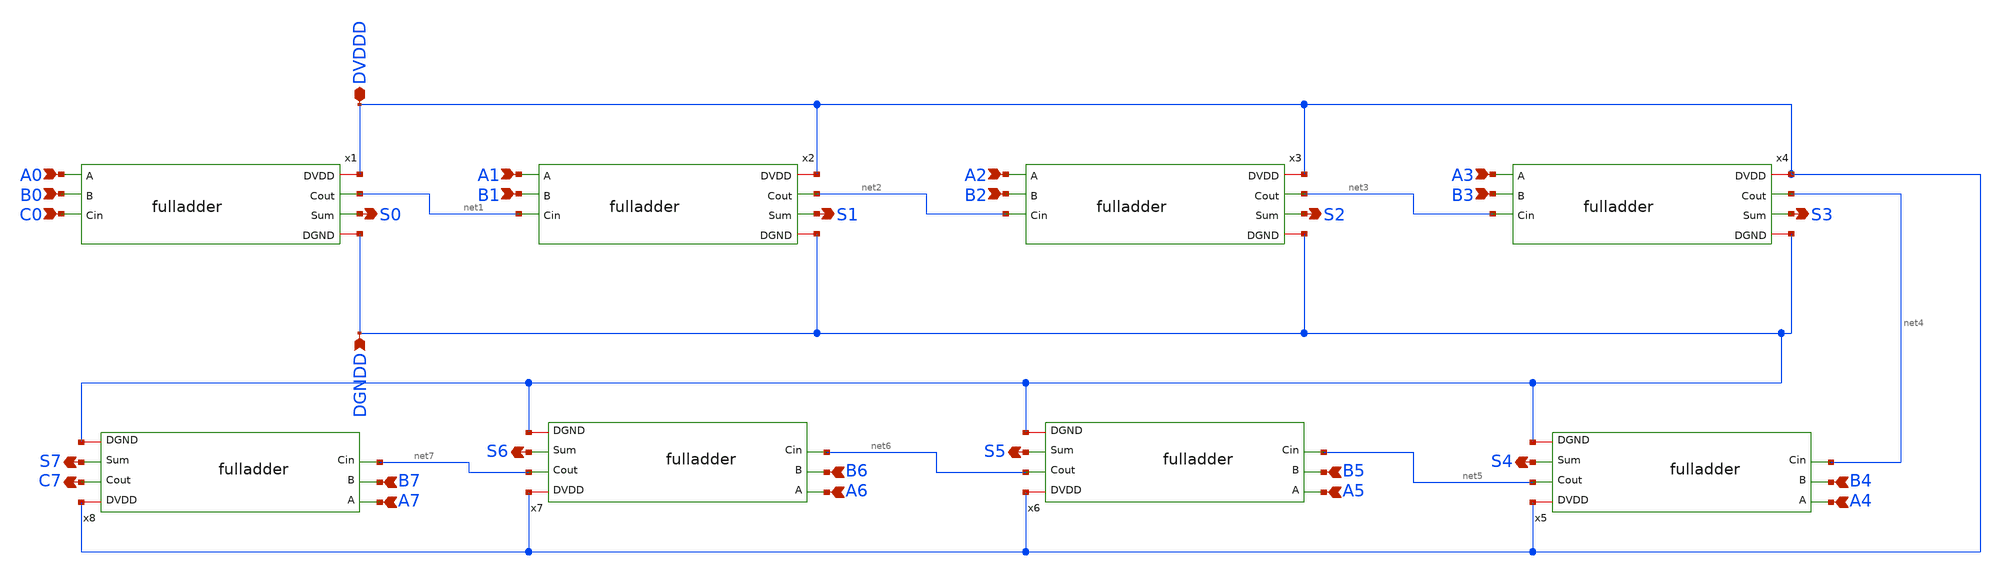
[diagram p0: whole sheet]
** sch_path: Tutorial_6/Part-B/rippleadder.sch
**.subckt rippleadder DVDDD DGNDD S0 S1 S2 S3 S4 S5 S6 S7 A0 A1 A2 A3 A4 A5 A6 A7 B1 B2 B0 B3 B4 B5
*+ B6 B7 C0 C7
*.iopin DVDDD
*.ipin DGNDD
*.opin S0
*.opin S1
*.opin S2
*.opin S3
*.opin S4
*.opin S5
*.opin S6
*.opin S7
*.ipin A0
*.ipin A1
*.ipin A2
*.ipin A3
*.ipin A4
*.ipin A5
*.ipin A6
*.ipin A7
*.ipin B1
*.ipin B2
*.ipin B0
*.ipin B3
*.ipin B4
*.ipin B5
*.ipin B6
*.ipin B7
*.ipin C0
*.opin C7
x1 DVDDD A0 B0 C0 net1 S0 DGNDD fulladder
x2 DVDDD A1 B1 net1 net2 S1 DGNDD fulladder
x3 DVDDD A2 B2 net2 net3 S2 DGNDD fulladder
x4 DVDDD A3 B3 net3 net4 S3 DGNDD fulladder
x5 DVDDD A4 B4 net4 net5 S4 DGNDD fulladder
x6 DVDDD A5 B5 net5 net6 S5 DGNDD fulladder
x7 DVDDD A6 B6 net6 net7 S6 DGNDD fulladder
x8 DVDDD A7 B7 net7 C7 S7 DGNDD fulladder
**.ends

* expanding   symbol:  fulladder.sym # of pins=7
** sym_path: Tutorial_6/Part-B/fulladder.sym
** sch_path: Tutorial_6/Part-B/fulladder.sch
.subckt fulladder DVDD A B Cin Cout Sum DGND
*.opin Cout
*.opin Sum
*.ipin A
*.ipin B
*.ipin Cin
*.iopin DVDD
*.iopin DGND
XM25 net3 A DVDD DVDD sky130_fd_pr__pfet_01v8 L=0.15 W=0.84 nf=1 ad='int((nf+1)/2) * W/nf * 0.29' as='int((nf+2)/2) * W/nf * 0.29'
+ pd='2*int((nf+1)/2) * (W/nf + 0.29)' ps='2*int((nf+2)/2) * (W/nf + 0.29)' nrd='0.29 / W' nrs='0.29 / W'
+ sa=0 sb=0 sd=0 mult=1 m=1
XM26 net3 A DVDD DVDD sky130_fd_pr__pfet_01v8 L=0.15 W=0.84 nf=1 ad='int((nf+1)/2) * W/nf * 0.29' as='int((nf+2)/2) * W/nf * 0.29'
+ pd='2*int((nf+1)/2) * (W/nf + 0.29)' ps='2*int((nf+2)/2) * (W/nf + 0.29)' nrd='0.29 / W' nrs='0.29 / W'
+ sa=0 sb=0 sd=0 mult=1 m=1
XM27 net2 A DVDD DVDD sky130_fd_pr__pfet_01v8 L=0.15 W=0.84 nf=1 ad='int((nf+1)/2) * W/nf * 0.29' as='int((nf+2)/2) * W/nf * 0.29'
+ pd='2*int((nf+1)/2) * (W/nf + 0.29)' ps='2*int((nf+2)/2) * (W/nf + 0.29)' nrd='0.29 / W' nrs='0.29 / W'
+ sa=0 sb=0 sd=0 mult=1 m=1
XM28 net2 A DVDD DVDD sky130_fd_pr__pfet_01v8 L=0.15 W=0.84 nf=1 ad='int((nf+1)/2) * W/nf * 0.29' as='int((nf+2)/2) * W/nf * 0.29'
+ pd='2*int((nf+1)/2) * (W/nf + 0.29)' ps='2*int((nf+2)/2) * (W/nf + 0.29)' nrd='0.29 / W' nrs='0.29 / W'
+ sa=0 sb=0 sd=0 mult=1 m=1
XM29 net2 B DVDD DVDD sky130_fd_pr__pfet_01v8 L=0.15 W=0.84 nf=1 ad='int((nf+1)/2) * W/nf * 0.29' as='int((nf+2)/2) * W/nf * 0.29'
+ pd='2*int((nf+1)/2) * (W/nf + 0.29)' ps='2*int((nf+2)/2) * (W/nf + 0.29)' nrd='0.29 / W' nrs='0.29 / W'
+ sa=0 sb=0 sd=0 mult=1 m=1
XM30 net2 B DVDD DVDD sky130_fd_pr__pfet_01v8 L=0.15 W=0.84 nf=1 ad='int((nf+1)/2) * W/nf * 0.29' as='int((nf+2)/2) * W/nf * 0.29'
+ pd='2*int((nf+1)/2) * (W/nf + 0.29)' ps='2*int((nf+2)/2) * (W/nf + 0.29)' nrd='0.29 / W' nrs='0.29 / W'
+ sa=0 sb=0 sd=0 mult=1 m=1
XM31 Cout B net3 DVDD sky130_fd_pr__pfet_01v8 L=0.15 W=0.84 nf=1 ad='int((nf+1)/2) * W/nf * 0.29' as='int((nf+2)/2) * W/nf * 0.29'
+ pd='2*int((nf+1)/2) * (W/nf + 0.29)' ps='2*int((nf+2)/2) * (W/nf + 0.29)' nrd='0.29 / W' nrs='0.29 / W'
+ sa=0 sb=0 sd=0 mult=1 m=1
XM32 Cout B net3 DVDD sky130_fd_pr__pfet_01v8 L=0.15 W=0.84 nf=1 ad='int((nf+1)/2) * W/nf * 0.29' as='int((nf+2)/2) * W/nf * 0.29'
+ pd='2*int((nf+1)/2) * (W/nf + 0.29)' ps='2*int((nf+2)/2) * (W/nf + 0.29)' nrd='0.29 / W' nrs='0.29 / W'
+ sa=0 sb=0 sd=0 mult=1 m=1
XM33 Cout Cin net2 DVDD sky130_fd_pr__pfet_01v8 L=0.15 W=0.84 nf=1 ad='int((nf+1)/2) * W/nf * 0.29' as='int((nf+2)/2) * W/nf * 0.29'
+ pd='2*int((nf+1)/2) * (W/nf + 0.29)' ps='2*int((nf+2)/2) * (W/nf + 0.29)' nrd='0.29 / W' nrs='0.29 / W'
+ sa=0 sb=0 sd=0 mult=1 m=1
XM34 Cout Cin net2 DVDD sky130_fd_pr__pfet_01v8 L=0.15 W=0.84 nf=1 ad='int((nf+1)/2) * W/nf * 0.29' as='int((nf+2)/2) * W/nf * 0.29'
+ pd='2*int((nf+1)/2) * (W/nf + 0.29)' ps='2*int((nf+2)/2) * (W/nf + 0.29)' nrd='0.29 / W' nrs='0.29 / W'
+ sa=0 sb=0 sd=0 mult=1 m=1
XM35 net6 A DVDD DVDD sky130_fd_pr__pfet_01v8 L=0.15 W=0.84 nf=1 ad='int((nf+1)/2) * W/nf * 0.29' as='int((nf+2)/2) * W/nf * 0.29'
+ pd='2*int((nf+1)/2) * (W/nf + 0.29)' ps='2*int((nf+2)/2) * (W/nf + 0.29)' nrd='0.29 / W' nrs='0.29 / W'
+ sa=0 sb=0 sd=0 mult=1 m=1
XM36 net6 A DVDD DVDD sky130_fd_pr__pfet_01v8 L=0.15 W=0.84 nf=1 ad='int((nf+1)/2) * W/nf * 0.29' as='int((nf+2)/2) * W/nf * 0.29'
+ pd='2*int((nf+1)/2) * (W/nf + 0.29)' ps='2*int((nf+2)/2) * (W/nf + 0.29)' nrd='0.29 / W' nrs='0.29 / W'
+ sa=0 sb=0 sd=0 mult=1 m=1
XM37 net6 B DVDD DVDD sky130_fd_pr__pfet_01v8 L=0.15 W=0.84 nf=1 ad='int((nf+1)/2) * W/nf * 0.29' as='int((nf+2)/2) * W/nf * 0.29'
+ pd='2*int((nf+1)/2) * (W/nf + 0.29)' ps='2*int((nf+2)/2) * (W/nf + 0.29)' nrd='0.29 / W' nrs='0.29 / W'
+ sa=0 sb=0 sd=0 mult=1 m=1
XM38 net6 B DVDD DVDD sky130_fd_pr__pfet_01v8 L=0.15 W=0.84 nf=1 ad='int((nf+1)/2) * W/nf * 0.29' as='int((nf+2)/2) * W/nf * 0.29'
+ pd='2*int((nf+1)/2) * (W/nf + 0.29)' ps='2*int((nf+2)/2) * (W/nf + 0.29)' nrd='0.29 / W' nrs='0.29 / W'
+ sa=0 sb=0 sd=0 mult=1 m=1
XM39 net6 Cin DVDD DVDD sky130_fd_pr__pfet_01v8 L=0.15 W=0.84 nf=1 ad='int((nf+1)/2) * W/nf * 0.29' as='int((nf+2)/2) * W/nf * 0.29'
+ pd='2*int((nf+1)/2) * (W/nf + 0.29)' ps='2*int((nf+2)/2) * (W/nf + 0.29)' nrd='0.29 / W' nrs='0.29 / W'
+ sa=0 sb=0 sd=0 mult=1 m=1
XM40 net6 Cin DVDD DVDD sky130_fd_pr__pfet_01v8 L=0.15 W=0.84 nf=1 ad='int((nf+1)/2) * W/nf * 0.29' as='int((nf+2)/2) * W/nf * 0.29'
+ pd='2*int((nf+1)/2) * (W/nf + 0.29)' ps='2*int((nf+2)/2) * (W/nf + 0.29)' nrd='0.29 / W' nrs='0.29 / W'
+ sa=0 sb=0 sd=0 mult=1 m=1
XM41 Sum Cout net6 DVDD sky130_fd_pr__pfet_01v8 L=0.15 W=0.84 nf=1 ad='int((nf+1)/2) * W/nf * 0.29' as='int((nf+2)/2) * W/nf * 0.29'
+ pd='2*int((nf+1)/2) * (W/nf + 0.29)' ps='2*int((nf+2)/2) * (W/nf + 0.29)' nrd='0.29 / W' nrs='0.29 / W'
+ sa=0 sb=0 sd=0 mult=1 m=1
XM42 Sum Cout net6 DVDD sky130_fd_pr__pfet_01v8 L=0.15 W=0.84 nf=1 ad='int((nf+1)/2) * W/nf * 0.29' as='int((nf+2)/2) * W/nf * 0.29'
+ pd='2*int((nf+1)/2) * (W/nf + 0.29)' ps='2*int((nf+2)/2) * (W/nf + 0.29)' nrd='0.29 / W' nrs='0.29 / W'
+ sa=0 sb=0 sd=0 mult=1 m=1
XM43 net7 A DVDD DVDD sky130_fd_pr__pfet_01v8 L=0.15 W=0.84 nf=1 ad='int((nf+1)/2) * W/nf * 0.29' as='int((nf+2)/2) * W/nf * 0.29'
+ pd='2*int((nf+1)/2) * (W/nf + 0.29)' ps='2*int((nf+2)/2) * (W/nf + 0.29)' nrd='0.29 / W' nrs='0.29 / W'
+ sa=0 sb=0 sd=0 mult=1 m=1
XM44 net7 A DVDD DVDD sky130_fd_pr__pfet_01v8 L=0.15 W=0.84 nf=1 ad='int((nf+1)/2) * W/nf * 0.29' as='int((nf+2)/2) * W/nf * 0.29'
+ pd='2*int((nf+1)/2) * (W/nf + 0.29)' ps='2*int((nf+2)/2) * (W/nf + 0.29)' nrd='0.29 / W' nrs='0.29 / W'
+ sa=0 sb=0 sd=0 mult=1 m=1
XM45 net7 A DVDD DVDD sky130_fd_pr__pfet_01v8 L=0.15 W=0.84 nf=1 ad='int((nf+1)/2) * W/nf * 0.29' as='int((nf+2)/2) * W/nf * 0.29'
+ pd='2*int((nf+1)/2) * (W/nf + 0.29)' ps='2*int((nf+2)/2) * (W/nf + 0.29)' nrd='0.29 / W' nrs='0.29 / W'
+ sa=0 sb=0 sd=0 mult=1 m=1
XM46 net8 B net7 DVDD sky130_fd_pr__pfet_01v8 L=0.15 W=0.84 nf=1 ad='int((nf+1)/2) * W/nf * 0.29' as='int((nf+2)/2) * W/nf * 0.29'
+ pd='2*int((nf+1)/2) * (W/nf + 0.29)' ps='2*int((nf+2)/2) * (W/nf + 0.29)' nrd='0.29 / W' nrs='0.29 / W'
+ sa=0 sb=0 sd=0 mult=1 m=1
XM47 net8 B net7 DVDD sky130_fd_pr__pfet_01v8 L=0.15 W=0.84 nf=1 ad='int((nf+1)/2) * W/nf * 0.29' as='int((nf+2)/2) * W/nf * 0.29'
+ pd='2*int((nf+1)/2) * (W/nf + 0.29)' ps='2*int((nf+2)/2) * (W/nf + 0.29)' nrd='0.29 / W' nrs='0.29 / W'
+ sa=0 sb=0 sd=0 mult=1 m=1
XM48 net8 B net7 DVDD sky130_fd_pr__pfet_01v8 L=0.15 W=0.84 nf=1 ad='int((nf+1)/2) * W/nf * 0.29' as='int((nf+2)/2) * W/nf * 0.29'
+ pd='2*int((nf+1)/2) * (W/nf + 0.29)' ps='2*int((nf+2)/2) * (W/nf + 0.29)' nrd='0.29 / W' nrs='0.29 / W'
+ sa=0 sb=0 sd=0 mult=1 m=1
XM49 Sum Cin net8 DVDD sky130_fd_pr__pfet_01v8 L=0.15 W=0.84 nf=1 ad='int((nf+1)/2) * W/nf * 0.29' as='int((nf+2)/2) * W/nf * 0.29'
+ pd='2*int((nf+1)/2) * (W/nf + 0.29)' ps='2*int((nf+2)/2) * (W/nf + 0.29)' nrd='0.29 / W' nrs='0.29 / W'
+ sa=0 sb=0 sd=0 mult=1 m=1
XM50 Sum Cin net8 DVDD sky130_fd_pr__pfet_01v8 L=0.15 W=0.84 nf=1 ad='int((nf+1)/2) * W/nf * 0.29' as='int((nf+2)/2) * W/nf * 0.29'
+ pd='2*int((nf+1)/2) * (W/nf + 0.29)' ps='2*int((nf+2)/2) * (W/nf + 0.29)' nrd='0.29 / W' nrs='0.29 / W'
+ sa=0 sb=0 sd=0 mult=1 m=1
XM51 Sum Cin net8 DVDD sky130_fd_pr__pfet_01v8 L=0.15 W=0.84 nf=1 ad='int((nf+1)/2) * W/nf * 0.29' as='int((nf+2)/2) * W/nf * 0.29'
+ pd='2*int((nf+1)/2) * (W/nf + 0.29)' ps='2*int((nf+2)/2) * (W/nf + 0.29)' nrd='0.29 / W' nrs='0.29 / W'
+ sa=0 sb=0 sd=0 mult=1 m=1
XM52 Cout A net1 DGND sky130_fd_pr__nfet_01v8 L=0.15 W=0.42 nf=1 ad='int((nf+1)/2) * W/nf * 0.29' as='int((nf+2)/2) * W/nf * 0.29'
+ pd='2*int((nf+1)/2) * (W/nf + 0.29)' ps='2*int((nf+2)/2) * (W/nf + 0.29)' nrd='0.29 / W' nrs='0.29 / W'
+ sa=0 sb=0 sd=0 mult=1 m=1
XM53 Cout A net1 DGND sky130_fd_pr__nfet_01v8 L=0.15 W=0.42 nf=1 ad='int((nf+1)/2) * W/nf * 0.29' as='int((nf+2)/2) * W/nf * 0.29'
+ pd='2*int((nf+1)/2) * (W/nf + 0.29)' ps='2*int((nf+2)/2) * (W/nf + 0.29)' nrd='0.29 / W' nrs='0.29 / W'
+ sa=0 sb=0 sd=0 mult=1 m=1
XM54 net1 B DGND DGND sky130_fd_pr__nfet_01v8 L=0.15 W=0.42 nf=1 ad='int((nf+1)/2) * W/nf * 0.29' as='int((nf+2)/2) * W/nf * 0.29'
+ pd='2*int((nf+1)/2) * (W/nf + 0.29)' ps='2*int((nf+2)/2) * (W/nf + 0.29)' nrd='0.29 / W' nrs='0.29 / W'
+ sa=0 sb=0 sd=0 mult=1 m=1
XM55 net1 B DGND DGND sky130_fd_pr__nfet_01v8 L=0.15 W=0.42 nf=1 ad='int((nf+1)/2) * W/nf * 0.29' as='int((nf+2)/2) * W/nf * 0.29'
+ pd='2*int((nf+1)/2) * (W/nf + 0.29)' ps='2*int((nf+2)/2) * (W/nf + 0.29)' nrd='0.29 / W' nrs='0.29 / W'
+ sa=0 sb=0 sd=0 mult=1 m=1
XM56 Cout Cin net4 DGND sky130_fd_pr__nfet_01v8 L=0.15 W=0.42 nf=1 ad='int((nf+1)/2) * W/nf * 0.29' as='int((nf+2)/2) * W/nf * 0.29'
+ pd='2*int((nf+1)/2) * (W/nf + 0.29)' ps='2*int((nf+2)/2) * (W/nf + 0.29)' nrd='0.29 / W' nrs='0.29 / W'
+ sa=0 sb=0 sd=0 mult=1 m=1
XM57 Cout Cin net4 DGND sky130_fd_pr__nfet_01v8 L=0.15 W=0.42 nf=1 ad='int((nf+1)/2) * W/nf * 0.29' as='int((nf+2)/2) * W/nf * 0.29'
+ pd='2*int((nf+1)/2) * (W/nf + 0.29)' ps='2*int((nf+2)/2) * (W/nf + 0.29)' nrd='0.29 / W' nrs='0.29 / W'
+ sa=0 sb=0 sd=0 mult=1 m=1
XM58 net4 A DGND DGND sky130_fd_pr__nfet_01v8 L=0.15 W=0.42 nf=1 ad='int((nf+1)/2) * W/nf * 0.29' as='int((nf+2)/2) * W/nf * 0.29'
+ pd='2*int((nf+1)/2) * (W/nf + 0.29)' ps='2*int((nf+2)/2) * (W/nf + 0.29)' nrd='0.29 / W' nrs='0.29 / W'
+ sa=0 sb=0 sd=0 mult=1 m=1
XM59 net4 A DGND DGND sky130_fd_pr__nfet_01v8 L=0.15 W=0.42 nf=1 ad='int((nf+1)/2) * W/nf * 0.29' as='int((nf+2)/2) * W/nf * 0.29'
+ pd='2*int((nf+1)/2) * (W/nf + 0.29)' ps='2*int((nf+2)/2) * (W/nf + 0.29)' nrd='0.29 / W' nrs='0.29 / W'
+ sa=0 sb=0 sd=0 mult=1 m=1
XM60 net4 B DGND DGND sky130_fd_pr__nfet_01v8 L=0.15 W=0.42 nf=1 ad='int((nf+1)/2) * W/nf * 0.29' as='int((nf+2)/2) * W/nf * 0.29'
+ pd='2*int((nf+1)/2) * (W/nf + 0.29)' ps='2*int((nf+2)/2) * (W/nf + 0.29)' nrd='0.29 / W' nrs='0.29 / W'
+ sa=0 sb=0 sd=0 mult=1 m=1
XM61 net4 B DGND DGND sky130_fd_pr__nfet_01v8 L=0.15 W=0.42 nf=1 ad='int((nf+1)/2) * W/nf * 0.29' as='int((nf+2)/2) * W/nf * 0.29'
+ pd='2*int((nf+1)/2) * (W/nf + 0.29)' ps='2*int((nf+2)/2) * (W/nf + 0.29)' nrd='0.29 / W' nrs='0.29 / W'
+ sa=0 sb=0 sd=0 mult=1 m=1
XM62 Sum Cout net5 GND sky130_fd_pr__nfet_01v8 L=0.15 W=0.42 nf=1 ad='int((nf+1)/2) * W/nf * 0.29' as='int((nf+2)/2) * W/nf * 0.29'
+ pd='2*int((nf+1)/2) * (W/nf + 0.29)' ps='2*int((nf+2)/2) * (W/nf + 0.29)' nrd='0.29 / W' nrs='0.29 / W'
+ sa=0 sb=0 sd=0 mult=1 m=1
XM63 Sum Cout net5 DGND sky130_fd_pr__nfet_01v8 L=0.15 W=0.42 nf=1 ad='int((nf+1)/2) * W/nf * 0.29' as='int((nf+2)/2) * W/nf * 0.29'
+ pd='2*int((nf+1)/2) * (W/nf + 0.29)' ps='2*int((nf+2)/2) * (W/nf + 0.29)' nrd='0.29 / W' nrs='0.29 / W'
+ sa=0 sb=0 sd=0 mult=1 m=1
XM64 net5 A DGND DGND sky130_fd_pr__nfet_01v8 L=0.15 W=0.42 nf=1 ad='int((nf+1)/2) * W/nf * 0.29' as='int((nf+2)/2) * W/nf * 0.29'
+ pd='2*int((nf+1)/2) * (W/nf + 0.29)' ps='2*int((nf+2)/2) * (W/nf + 0.29)' nrd='0.29 / W' nrs='0.29 / W'
+ sa=0 sb=0 sd=0 mult=1 m=1
XM65 net5 A DGND DGND sky130_fd_pr__nfet_01v8 L=0.15 W=0.42 nf=1 ad='int((nf+1)/2) * W/nf * 0.29' as='int((nf+2)/2) * W/nf * 0.29'
+ pd='2*int((nf+1)/2) * (W/nf + 0.29)' ps='2*int((nf+2)/2) * (W/nf + 0.29)' nrd='0.29 / W' nrs='0.29 / W'
+ sa=0 sb=0 sd=0 mult=1 m=1
XM66 net5 B DGND DGND sky130_fd_pr__nfet_01v8 L=0.15 W=0.42 nf=1 ad='int((nf+1)/2) * W/nf * 0.29' as='int((nf+2)/2) * W/nf * 0.29'
+ pd='2*int((nf+1)/2) * (W/nf + 0.29)' ps='2*int((nf+2)/2) * (W/nf + 0.29)' nrd='0.29 / W' nrs='0.29 / W'
+ sa=0 sb=0 sd=0 mult=1 m=1
XM67 net5 B DGND DGND sky130_fd_pr__nfet_01v8 L=0.15 W=0.42 nf=1 ad='int((nf+1)/2) * W/nf * 0.29' as='int((nf+2)/2) * W/nf * 0.29'
+ pd='2*int((nf+1)/2) * (W/nf + 0.29)' ps='2*int((nf+2)/2) * (W/nf + 0.29)' nrd='0.29 / W' nrs='0.29 / W'
+ sa=0 sb=0 sd=0 mult=1 m=1
XM68 net5 Cin DGND DGND sky130_fd_pr__nfet_01v8 L=0.15 W=0.42 nf=1 ad='int((nf+1)/2) * W/nf * 0.29' as='int((nf+2)/2) * W/nf * 0.29'
+ pd='2*int((nf+1)/2) * (W/nf + 0.29)' ps='2*int((nf+2)/2) * (W/nf + 0.29)' nrd='0.29 / W' nrs='0.29 / W'
+ sa=0 sb=0 sd=0 mult=1 m=1
XM69 net5 Cin DGND DGND sky130_fd_pr__nfet_01v8 L=0.15 W=0.42 nf=1 ad='int((nf+1)/2) * W/nf * 0.29' as='int((nf+2)/2) * W/nf * 0.29'
+ pd='2*int((nf+1)/2) * (W/nf + 0.29)' ps='2*int((nf+2)/2) * (W/nf + 0.29)' nrd='0.29 / W' nrs='0.29 / W'
+ sa=0 sb=0 sd=0 mult=1 m=1
XM70 Sum Cin net9 DGND sky130_fd_pr__nfet_01v8 L=0.15 W=0.42 nf=1 ad='int((nf+1)/2) * W/nf * 0.29' as='int((nf+2)/2) * W/nf * 0.29'
+ pd='2*int((nf+1)/2) * (W/nf + 0.29)' ps='2*int((nf+2)/2) * (W/nf + 0.29)' nrd='0.29 / W' nrs='0.29 / W'
+ sa=0 sb=0 sd=0 mult=1 m=1
XM71 Sum Cin net9 DGND sky130_fd_pr__nfet_01v8 L=0.15 W=0.42 nf=1 ad='int((nf+1)/2) * W/nf * 0.29' as='int((nf+2)/2) * W/nf * 0.29'
+ pd='2*int((nf+1)/2) * (W/nf + 0.29)' ps='2*int((nf+2)/2) * (W/nf + 0.29)' nrd='0.29 / W' nrs='0.29 / W'
+ sa=0 sb=0 sd=0 mult=1 m=1
XM72 net9 A net10 DGND sky130_fd_pr__nfet_01v8 L=0.15 W=0.42 nf=1 ad='int((nf+1)/2) * W/nf * 0.29' as='int((nf+2)/2) * W/nf * 0.29'
+ pd='2*int((nf+1)/2) * (W/nf + 0.29)' ps='2*int((nf+2)/2) * (W/nf + 0.29)' nrd='0.29 / W' nrs='0.29 / W'
+ sa=0 sb=0 sd=0 mult=1 m=1
XM73 net9 A net10 DGND sky130_fd_pr__nfet_01v8 L=0.15 W=0.42 nf=1 ad='int((nf+1)/2) * W/nf * 0.29' as='int((nf+2)/2) * W/nf * 0.29'
+ pd='2*int((nf+1)/2) * (W/nf + 0.29)' ps='2*int((nf+2)/2) * (W/nf + 0.29)' nrd='0.29 / W' nrs='0.29 / W'
+ sa=0 sb=0 sd=0 mult=1 m=1
XM74 net10 B DGND DGND sky130_fd_pr__nfet_01v8 L=0.15 W=0.42 nf=1 ad='int((nf+1)/2) * W/nf * 0.29' as='int((nf+2)/2) * W/nf * 0.29'
+ pd='2*int((nf+1)/2) * (W/nf + 0.29)' ps='2*int((nf+2)/2) * (W/nf + 0.29)' nrd='0.29 / W' nrs='0.29 / W'
+ sa=0 sb=0 sd=0 mult=1 m=1
XM75 net10 B DGND DGND sky130_fd_pr__nfet_01v8 L=0.15 W=0.42 nf=1 ad='int((nf+1)/2) * W/nf * 0.29' as='int((nf+2)/2) * W/nf * 0.29'
+ pd='2*int((nf+1)/2) * (W/nf + 0.29)' ps='2*int((nf+2)/2) * (W/nf + 0.29)' nrd='0.29 / W' nrs='0.29 / W'
+ sa=0 sb=0 sd=0 mult=1 m=1
XM76 Sum Cin net9 DGND sky130_fd_pr__nfet_01v8 L=0.15 W=0.42 nf=1 ad='int((nf+1)/2) * W/nf * 0.29' as='int((nf+2)/2) * W/nf * 0.29'
+ pd='2*int((nf+1)/2) * (W/nf + 0.29)' ps='2*int((nf+2)/2) * (W/nf + 0.29)' nrd='0.29 / W' nrs='0.29 / W'
+ sa=0 sb=0 sd=0 mult=1 m=1
XM77 net9 A net10 DGND sky130_fd_pr__nfet_01v8 L=0.15 W=0.42 nf=1 ad='int((nf+1)/2) * W/nf * 0.29' as='int((nf+2)/2) * W/nf * 0.29'
+ pd='2*int((nf+1)/2) * (W/nf + 0.29)' ps='2*int((nf+2)/2) * (W/nf + 0.29)' nrd='0.29 / W' nrs='0.29 / W'
+ sa=0 sb=0 sd=0 mult=1 m=1
XM78 net10 B DGND DGND sky130_fd_pr__nfet_01v8 L=0.15 W=0.42 nf=1 ad='int((nf+1)/2) * W/nf * 0.29' as='int((nf+2)/2) * W/nf * 0.29'
+ pd='2*int((nf+1)/2) * (W/nf + 0.29)' ps='2*int((nf+2)/2) * (W/nf + 0.29)' nrd='0.29 / W' nrs='0.29 / W'
+ sa=0 sb=0 sd=0 mult=1 m=1
.ends

.GLOBAL GND
.end
